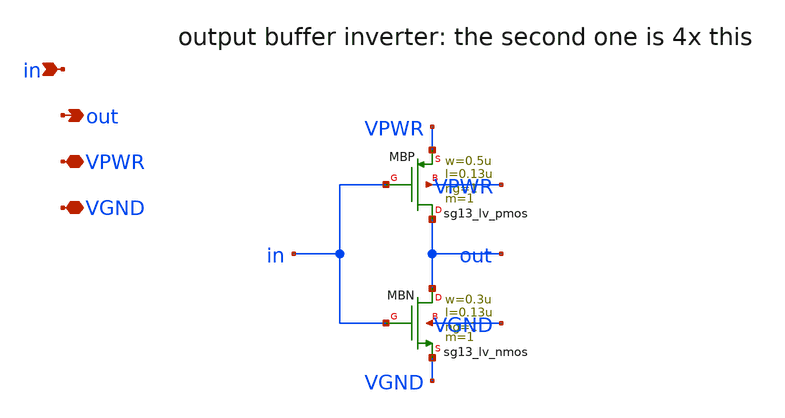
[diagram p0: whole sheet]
** sch_path: analog/xschem/csro_inv.sch
**.subckt csro_inv in out VPWR VGND
*.ipin in
*.opin out
*.iopin VPWR
*.iopin VGND
XMBP out in VPWR VPWR sg13_lv_pmos w=0.5u l=0.13u ng=1 m=1 mm_ok=1
XMBN out in VGND VGND sg13_lv_nmos w=0.3u l=0.13u ng=1 m=1 mm_ok=1
**.ends
.end
